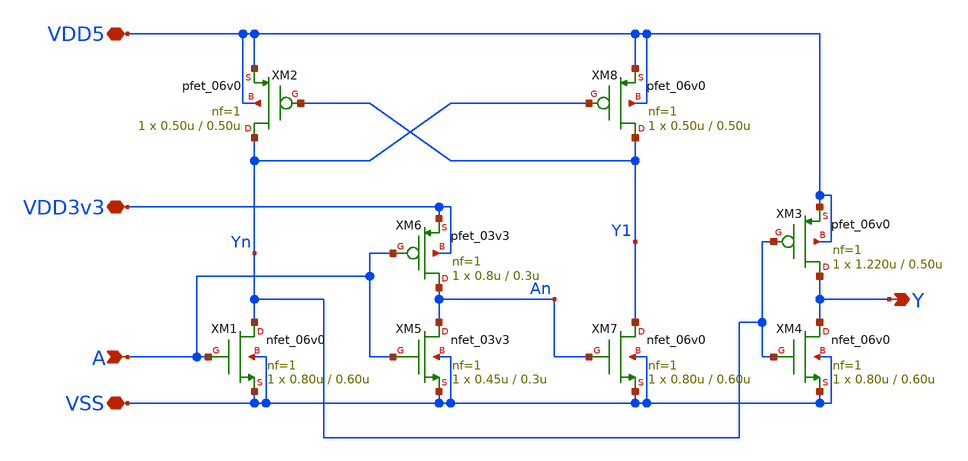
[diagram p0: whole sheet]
** sch_path: designs/libs/core_digital/gf180mcu_osu_sc_gp9t3v3/cells/lshifup/gf180mcu_osu_sc_gp9t3v3_lshifup.sch
**.subckt gf180mcu_osu_sc_gp9t3v3_lshifup A Y VDD5 VDD3v3 VSS
*.ipin A
*.opin Y
*.iopin VDD5
*.iopin VDD3v3
*.iopin VSS
XM1 Yn A VSS VSS nfet_06v0 L=0.60u W=0.80u nf=1 ad='int((nf+1)/2) * W/nf * 0.18u' as='int((nf+2)/2) * W/nf * 0.18u'
+ pd='2*int((nf+1)/2) * (W/nf + 0.18u)' ps='2*int((nf+2)/2) * (W/nf + 0.18u)' nrd='0.18u / W' nrs='0.18u / W'
+ sa=0 sb=0 sd=0 m=1
XM2 Yn Y1 VDD5 VDD5 pfet_06v0 L=0.50u W=0.50u nf=1 ad='int((nf+1)/2) * W/nf * 0.18u' as='int((nf+2)/2) * W/nf * 0.18u'
+ pd='2*int((nf+1)/2) * (W/nf + 0.18u)' ps='2*int((nf+2)/2) * (W/nf + 0.18u)' nrd='0.18u / W' nrs='0.18u / W'
+ sa=0 sb=0 sd=0 m=1
XM3 Y Yn VDD5 VDD5 pfet_06v0 L=0.50u W=1.220u nf=1 ad='int((nf+1)/2) * W/nf * 0.18u' as='int((nf+2)/2) * W/nf * 0.18u'
+ pd='2*int((nf+1)/2) * (W/nf + 0.18u)' ps='2*int((nf+2)/2) * (W/nf + 0.18u)' nrd='0.18u / W' nrs='0.18u / W'
+ sa=0 sb=0 sd=0 m=1
XM4 Y Yn VSS VSS nfet_06v0 L=0.60u W=0.80u nf=1 ad='int((nf+1)/2) * W/nf * 0.18u' as='int((nf+2)/2) * W/nf * 0.18u'
+ pd='2*int((nf+1)/2) * (W/nf + 0.18u)' ps='2*int((nf+2)/2) * (W/nf + 0.18u)' nrd='0.18u / W' nrs='0.18u / W'
+ sa=0 sb=0 sd=0 m=1
XM5 An A VSS VSS nfet_03v3 L=0.3u W=0.45u nf=1 ad='int((nf+1)/2) * W/nf * 0.18u' as='int((nf+2)/2) * W/nf * 0.18u'
+ pd='2*int((nf+1)/2) * (W/nf + 0.18u)' ps='2*int((nf+2)/2) * (W/nf + 0.18u)' nrd='0.18u / W' nrs='0.18u / W'
+ sa=0 sb=0 sd=0 m=1
XM6 An A VDD3v3 VDD3v3 pfet_03v3 L=0.3u W=0.8u nf=1 ad='int((nf+1)/2) * W/nf * 0.18u' as='int((nf+2)/2) * W/nf * 0.18u'
+ pd='2*int((nf+1)/2) * (W/nf + 0.18u)' ps='2*int((nf+2)/2) * (W/nf + 0.18u)' nrd='0.18u / W' nrs='0.18u / W'
+ sa=0 sb=0 sd=0 m=1
XM7 Y1 An VSS VSS nfet_06v0 L=0.60u W=0.80u nf=1 ad='int((nf+1)/2) * W/nf * 0.18u' as='int((nf+2)/2) * W/nf * 0.18u'
+ pd='2*int((nf+1)/2) * (W/nf + 0.18u)' ps='2*int((nf+2)/2) * (W/nf + 0.18u)' nrd='0.18u / W' nrs='0.18u / W'
+ sa=0 sb=0 sd=0 m=1
XM8 Y1 Yn VDD5 VDD5 pfet_06v0 L=0.50u W=0.50u nf=1 ad='int((nf+1)/2) * W/nf * 0.18u' as='int((nf+2)/2) * W/nf * 0.18u'
+ pd='2*int((nf+1)/2) * (W/nf + 0.18u)' ps='2*int((nf+2)/2) * (W/nf + 0.18u)' nrd='0.18u / W' nrs='0.18u / W'
+ sa=0 sb=0 sd=0 m=1
**.ends
.end
